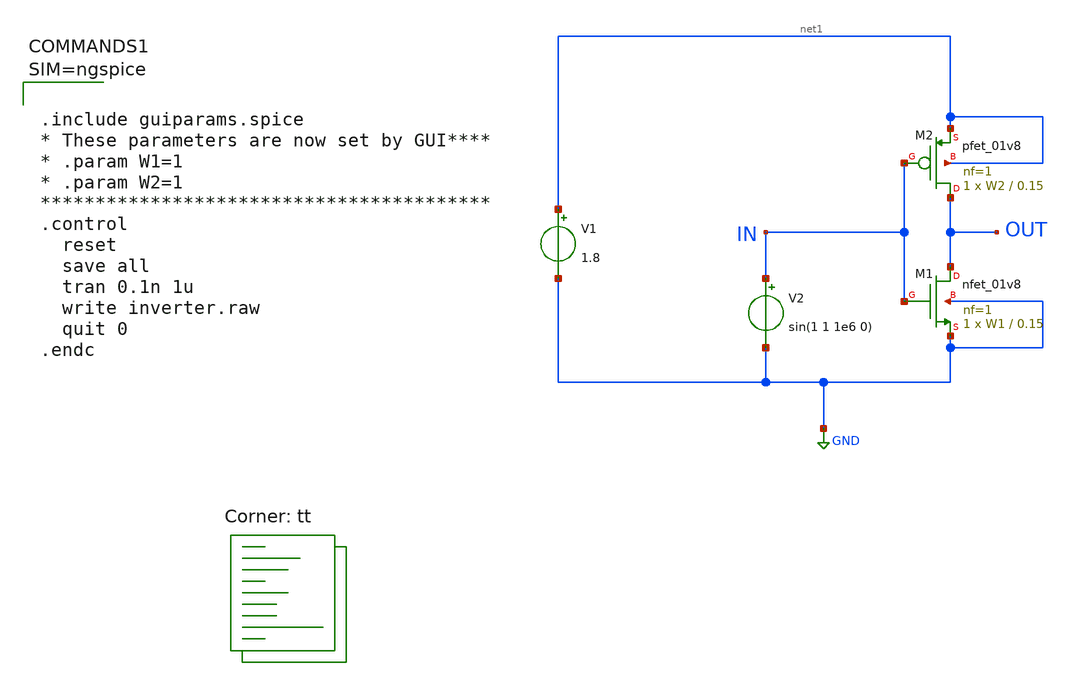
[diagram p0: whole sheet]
** sch_path: inverter/xschem/inverter.sch
**.subckt inverter
XM1 OUT IN GND GND sky130_fd_pr__nfet_01v8 L=0.15 W=W1 nf=1 ad='int((1 + 1)/2) * W1 / 1 * 0.29' as='int((1 + 2)/2) * W1 / 1 * 0.29'
+ pd='2*int((1 + 1)/2) * (W1 / 1 + 0.29)' ps='2*int((1 + 2)/2) * (W1 / 1 + 0.29)' nrd='0.29 / W1 ' nrs='0.29 / W1 '
+ sa=0 sb=0 sd=0 mult=1 m=1
XM2 OUT IN net1 net1 sky130_fd_pr__pfet_01v8 L=0.15 W=W2 nf=1 ad='int((nf+1)/2) * W/nf * 0.29' as='int((nf+2)/2) * W/nf * 0.29'
+ pd='2*int((nf+1)/2) * (W/nf + 0.29)' ps='2*int((nf+2)/2) * (W/nf + 0.29)' nrd='0.29 / W' nrs='0.29 / W'
+ sa=0 sb=0 sd=0 mult=1 m=1
V1 net1 GND 1.8
V2 IN GND sin(1 1 1e6 0)
**** begin user architecture code
.lib $::SKYWATER_MODELS/sky130.lib.spice tt



.include guiparams.spice
* These parameters are now set by GUI****
* .param W1=1
* .param W2=1
*****************************************
.control
  reset
  save all
  tran 0.1n 1u
  write inverter.raw
  quit 0
.endc



**** end user architecture code
**.ends
.GLOBAL GND
.end
